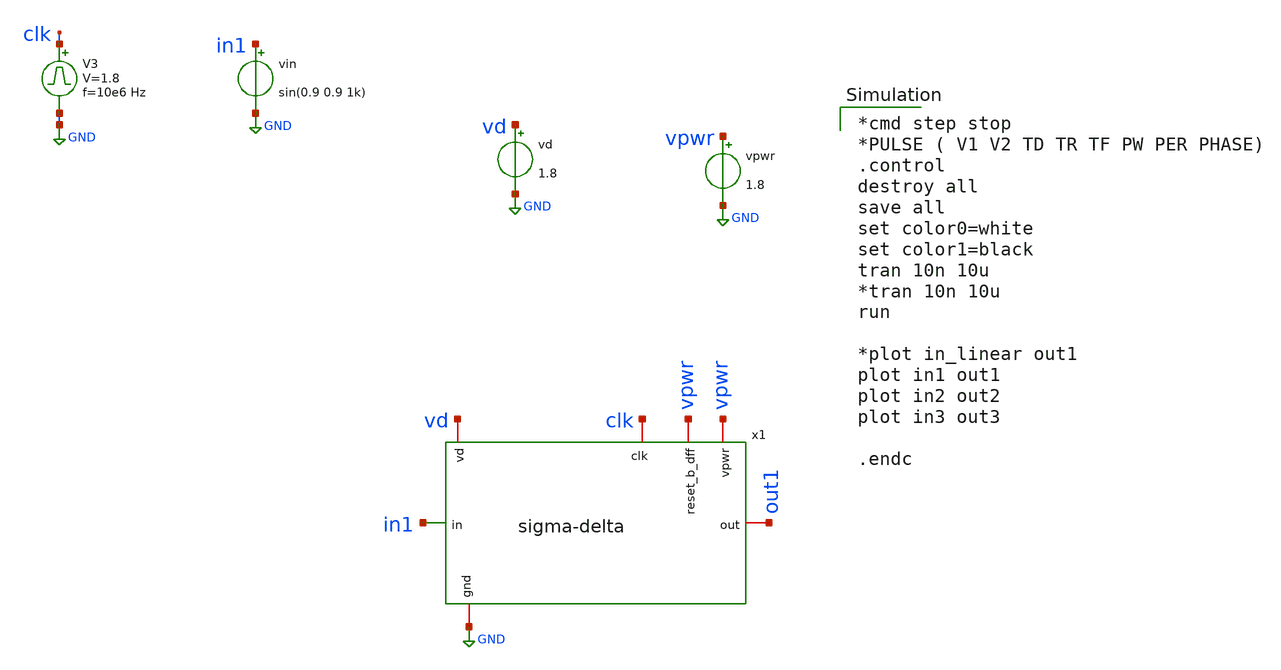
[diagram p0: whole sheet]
** sch_path: sigma-delta_modulator/xschem/sigma_tb-tran-sin.sch
* Copyright 2020 Stefan Frederik Schippers
* Licensed under the Apache License, Version 2.0 (the "License");
* you may not use this file except in compliance with the License.
* You may obtain a copy of the License at
* https://www.apache.org/licenses/LICENSE-2.0
* Unless required by applicable law or agreed to in writing, software
* distributed under the License is distributed on an "AS IS" BASIS,
* WITHOUT WARRANTIES OR CONDITIONS OF ANY KIND, either express or implied.
* See the License for the specific language governing permissions and
* limitations under the License.
**.subckt sigma_tb-tran-sin
vin in1 GND sin(0.9 0.9 1k)
vpwr vpwr GND 1.8
V3 clk GND pulse 0 1.8 '0.495/ 10e6 ' '0.01/10e6 ' '0.01/10e6 ' '0.49/10e6 ' '1/10e6 '
vd vd GND 1.8
x1 vpwr clk out1 in1 vpwr GND vd sigma-delta
**** begin user architecture code

*cmd step stop
*PULSE ( V1 V2 TD TR TF PW PER PHASE)
.control
destroy all
save all
set color0=white
set color1=black
tran 10n 10u
*tran 10n 10u
run

*plot in_linear out1
plot in1 out1
plot in2 out2
plot in3 out3

.endc

 .lib $::SKYWATER_MODELS/sky130.lib.spice tt
.include $::SKYWATER_STDCELLS/sky130_fd_sc_hd.spice

**** end user architecture code
**.ends

* expanding   symbol:  /foss/designs/temp-sensor/sigma-delta_modulator/xschem/sigma-delta.sym # of
*+ pins=7
** sym_path: sigma-delta_modulator/xschem/sigma-delta.sym
** sch_path: sigma-delta_modulator/xschem/sigma-delta.sch
.subckt sigma-delta vpwr clk out in reset_b_dff gnd vd
*.ipin in
*.iopin gnd
*.iopin clk
*.iopin out
*.iopin reset_b_dff
*.iopin vpwr
*.iopin vd
XR2 Q in_int gnd sky130_fd_pr__res_xhigh_po_0p35 L=36 mult=1 m=1
XR1 in_int in gnd sky130_fd_pr__res_xhigh_po_0p35 L=36 mult=1 m=1
XN1 out_comp in_comp gnd gnd sky130_fd_pr__nfet_01v8 L=0.15 W=1 nf=1 ad='int((nf+1)/2) * W/nf * 0.29'
+ as='int((nf+2)/2) * W/nf * 0.29' pd='2*int((nf+1)/2) * (W/nf + 0.29)' ps='2*int((nf+2)/2) * (W/nf + 0.29)'
+ nrd='0.29 / W' nrs='0.29 / W' sa=0 sb=0 sd=0 mult=1 m=1
XP1 out_comp in_comp vd vd sky130_fd_pr__pfet_01v8 L=0.15 W=3 nf=1 ad='int((nf+1)/2) * W/nf * 0.29' as='int((nf+2)/2) * W/nf * 0.29'
+ pd='2*int((nf+1)/2) * (W/nf + 0.29)' ps='2*int((nf+2)/2) * (W/nf + 0.29)' nrd='0.29 / W' nrs='0.29 / W'
+ sa=0 sb=0 sd=0 mult=1 m=1
x1 clk out_comp reset_b_dff GND GND VPWR VPWR Q out sky130_fd_sc_hd__dfrbp_1
XR3 in_comp in_int gnd sky130_fd_pr__res_xhigh_po_0p35 L=18 mult=1 m=1
XC1 in_int gnd sky130_fd_pr__cap_mim_m3_2 W=27.196 L=27.196 MF=1 m=1
XC2 in_comp gnd sky130_fd_pr__cap_mim_m3_2 W=27.196 L=27.196 MF=1 m=1
**** begin user architecture code

.include /foss/pdks/sky130A/libs.ref/sky130_fd_sc_hd/spice/sky130_fd_sc_hd.spice


**** end user architecture code
.ends

.GLOBAL GND
.end
